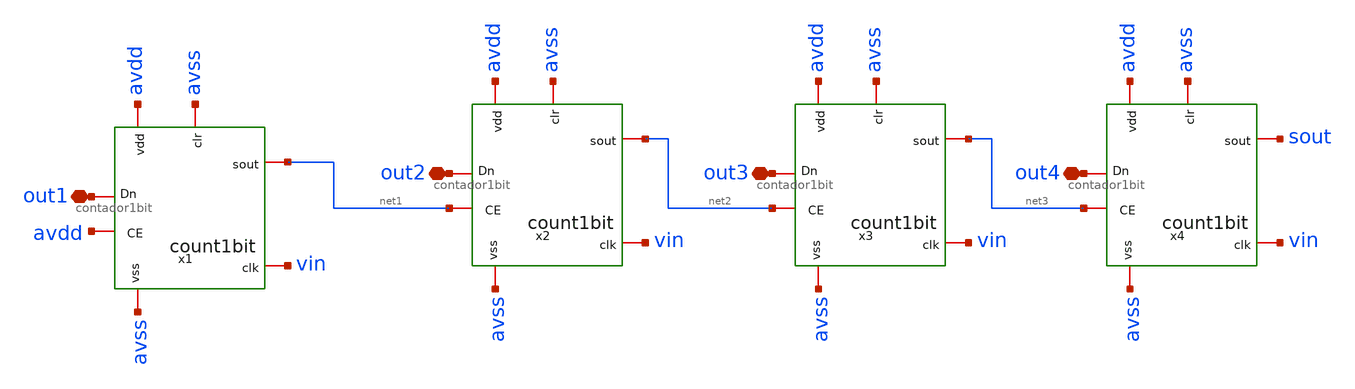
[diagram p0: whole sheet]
** sch_path: verification/testbenches/countador1bit/contador1bit.sch
**.subckt contador1bit out1 out2 out3 out4
*.iopin out1
*.iopin out2
*.iopin out3
*.iopin out4
x1 avss out1 avdd vin avdd avss net1 contador1bit
x2 avss out2 net1 vin avdd avss net2 contador1bit
x3 avss out3 net2 vin avdd avss net3 contador1bit
x4 avss out4 net3 vin avdd avss sout contador1bit
**.ends
.end
